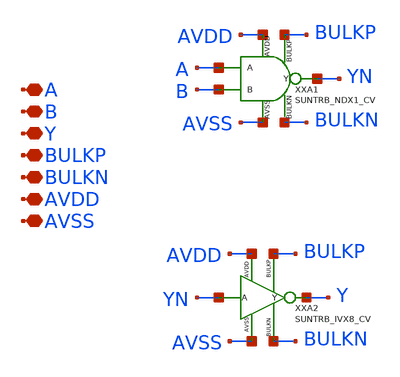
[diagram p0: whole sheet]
** sch_path: ip/sun_trb_sky130nm/design/SUN_TRB_SKY130NM/SUNTRB_ANX8_CV.sch
**.subckt SUNTRB_ANX8_CV A B Y BULKP BULKN AVDD AVSS
*.iopin A
*.iopin B
*.iopin Y
*.iopin BULKP
*.iopin BULKN
*.iopin AVDD
*.iopin AVSS
XXA1 A B YN BULKP BULKN AVDD AVSS SUNTRB_NDX1_CV xoffset=0 yoffset=0 angle=0
XXA2 YN Y BULKP BULKN AVDD AVSS SUNTRB_IVX8_CV xoffset=0 yoffset=0 angle=0
**.ends
.end
